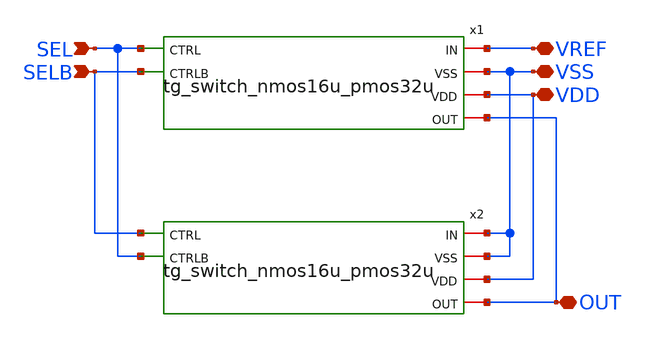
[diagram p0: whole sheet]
** sch_path: designs/libs/core_matchmaker/ref_sel_2to1_nmos16u_pmos32u/ref_sel_2to1_nmos16u_pmos32u.sch
**.subckt ref_sel_2to1_nmos16u_pmos32u VREF VSS VDD OUT SEL SELB
*.iopin VREF
*.iopin VSS
*.iopin VDD
*.iopin OUT
*.ipin SEL
*.ipin SELB
x1 VREF VSS VDD SEL SELB OUT tg_switch_nmos16u_pmos32u
x2 VSS VSS VDD SELB SEL OUT tg_switch_nmos16u_pmos32u
**.ends
.end
